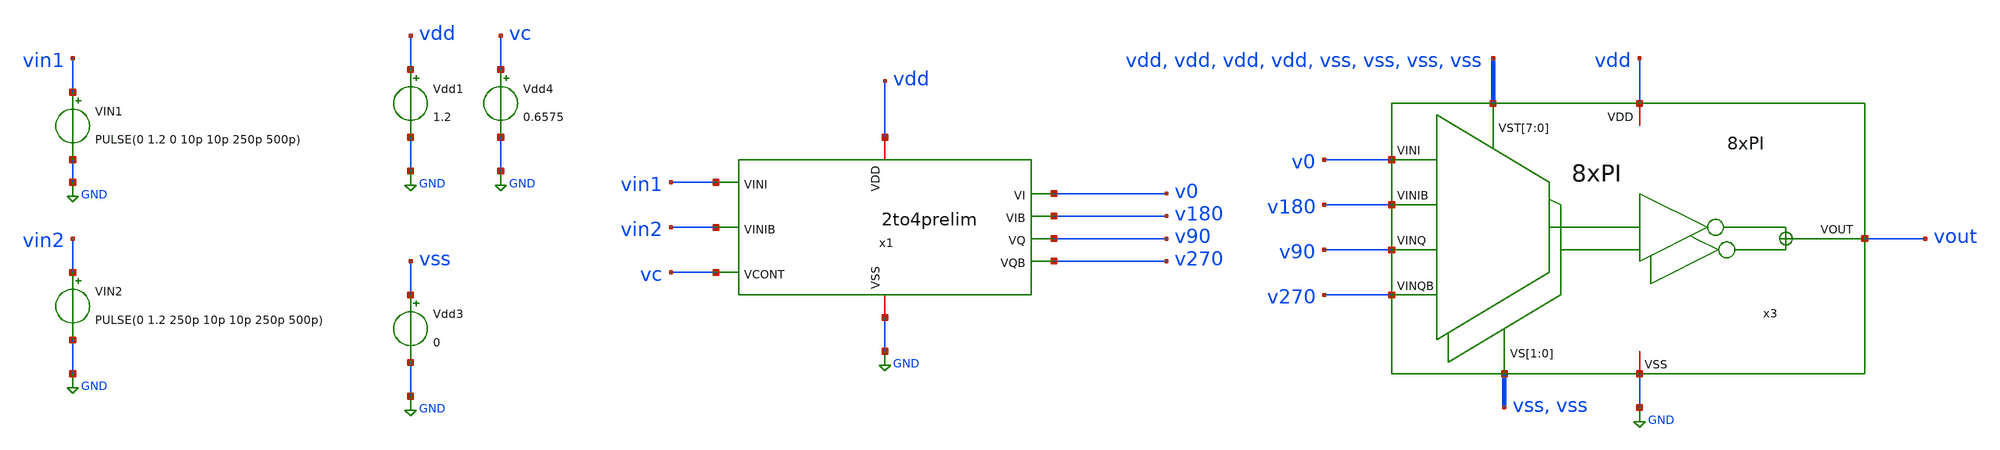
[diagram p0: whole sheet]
** sch_path: 2to4/tb_2to4prelim.sch
**.subckt tb_2to4prelim
x1 vdd v270 v90 vin1 GND vc v180 v0 vin2 2to4prelim
Vdd1 vdd GND 1.2
VIN1 vin1 GND PULSE(0 1.2 0 10p 10p 250p 500p)
VIN2 vin2 GND PULSE(0 1.2 250p 10p 10p 250p 500p)
Vdd4 vc GND 0.6575
x3 v0 v180 v90 v270 vss vss vdd vdd vdd vdd vss vss vss vss vout vdd GND 8xPI
Vdd3 vss GND 0
**** begin user architecture code


.save v(vin1) v(v0) v(v90) v(v270) v(v180) v(vin2) v(vout)

.tran 5p 3n
.save all

.control
run
set color0=white
write tran_logic.raw

* --- MEDICIONES DE FASE Y RETARDO (Usando v90) ---
* Periodo Entrada (Ref)
*meas tran T_p90 TRIG v(vin1) VAL=0.6 RISE=3 TARG v(vin1) VAL=0.6 RISE=4

* Retardo (Entrada vs v90)
*meas tran T_d90 TRIG v(vin1) VAL=0.6 RISE=3 TARG v(v90) VAL=0.6 RISE=3

* Calculo Fase
*let Phase_D90= (T_d90 / T_p90) * 360

*print T_p90
*print T_d90
*print Phase_D90


* --- DUTY CYCLE (Usando v90) ---
* Periodo Salida
*meas tran T_pe90 TRIG v(v90) VAL=0.6 RISE=2 TARG v(v90) VAL=0.6 RISE=3

* Tiempo en ALTO (Ton)
* Desde que sube (RISE=2) hasta que baja (FALL=2)
*meas tran T_h90 TRIG v(v90) VAL=0.6 RISE=2 TARG v(v90) VAL=0.6 FALL=2

* Tiempo en BAJO (Toff)
* Desde que baja (FALL=2) hasta que sube de nuevo (RISE=3)
*meas tran T_l90 TRIG v(v90) VAL=0.6 FALL=2 TARG v(v90) VAL=0.6 RISE=3

*let Duty_H90 = (T_h90 / T_pe90) * 100
*let Duty_L90 = (T_l90 / T_pe90) * 100

*print Duty_H90
*print Duty_L90

meas tran SKEW0_90 TRIG v(v0) VAL=0.6 RISE=3 TARG v(v90) VAL=0.6 RISE=4
meas tran SKEW90_180 TRIG v(v90) VAL=0.6 RISE=3 TARG v(v180) VAL=0.6 RISE=3
meas tran SKEW180_270 TRIG v(v180) VAL=0.6 RISE=3 TARG v(v270) VAL=0.6 RISE=3
meas tran SKEW270_0 TRIG v(v270) VAL=0.6 RISE=3 TARG v(v0) VAL=0.6 RISE=3

meas tran T90 TRIG v(v90) VAL=0.6 RISE=3 TARG v(v90) VAL=0.6 RISE=4
meas tran T180 TRIG v(v180) VAL=0.6 RISE=3 TARG v(v180) VAL=0.6 RISE=4
meas tran T270 TRIG v(v270) VAL=0.6 RISE=3 TARG v(v270) VAL=0.6 RISE=4
meas tran T0 TRIG v(v0) VAL=0.6 RISE=3 TARG v(v0) VAL=0.6 RISE=4

let phase0_90 = (SKEW0_90 / 500p) * 360
let phase90_180 = (SKEW90_180 / 500p) * 360
let phase180_270 = (SKEW180_270 / 500p) * 360
let phase270_0 = (SKEW270_0 / 500p) * 360


meas tran PW0 TRIG v(v0) VAL=0.6 RISE=3 TARG v(v0) VAL=0.6 FALL=4
meas tran PW90 TRIG v(v90) VAL=0.6 RISE=3 TARG v(v90) VAL=0.6 FALL=4
meas tran PW180 TRIG v(v180) VAL=0.6 RISE=3 TARG v(v180) VAL=0.6 FALL=4
meas tran PW270 TRIG v(v270) VAL=0.6 RISE=3 TARG v(v270) VAL=0.6 FALL=4

print SKEW0_90 SKEW90_180 SKEW180_270 SKEW270_0 phase0_90 phase90_180 phase180_270 phase270_0 PW0
+ PW90 PW180 PW270

.endc



.lib cornerMOSlv.lib mos_tt
.include /foss/pdks/ihp-sg13g2/libs.ref/sg13g2_stdcell/spice/sg13g2_stdcell.spice


**** end user architecture code
**.ends
.GLOBAL GND
.end
